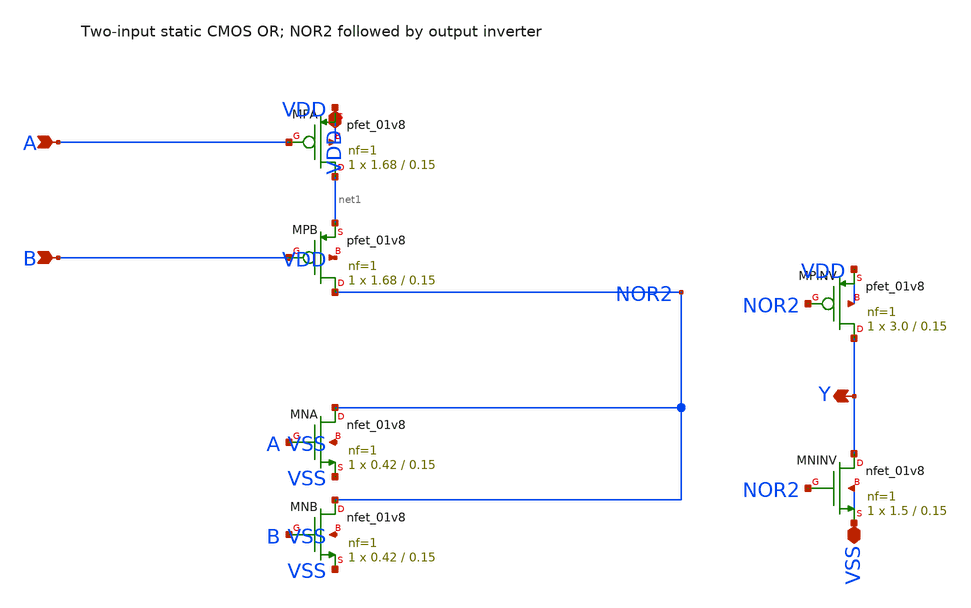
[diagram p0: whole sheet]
** sch_path: cells/control/phase_or2.sch
**.subckt phase_or2 VDD A B Y VSS
*.iopin VDD
*.ipin A
*.ipin B
*.opin Y
*.iopin VSS
XMPA net1 A VDD VDD sky130_fd_pr__pfet_01v8 L=0.15 W=1.68 nf=1 ad='int((nf+1)/2) * W/nf * 0.29' as='int((nf+2)/2) * W/nf * 0.29'
+ pd='2*int((nf+1)/2) * (W/nf + 0.29)' ps='2*int((nf+2)/2) * (W/nf + 0.29)' nrd='0.29 / W' nrs='0.29 / W'
+ sa=0 sb=0 sd=0 mult=1 m=1
XMPB NOR2 B net1 VDD sky130_fd_pr__pfet_01v8 L=0.15 W=1.68 nf=1 ad='int((nf+1)/2) * W/nf * 0.29' as='int((nf+2)/2) * W/nf * 0.29'
+ pd='2*int((nf+1)/2) * (W/nf + 0.29)' ps='2*int((nf+2)/2) * (W/nf + 0.29)' nrd='0.29 / W' nrs='0.29 / W'
+ sa=0 sb=0 sd=0 mult=1 m=1
XMNA NOR2 A VSS VSS sky130_fd_pr__nfet_01v8 L=0.15 W=0.42 nf=1 ad='int((1 + 1)/2) * 0.42 / 1 * 0.29'
+ as='int((1 + 2)/2) * 0.42 / 1 * 0.29' pd='2*int((1 + 1)/2) * (0.42 / 1 + 0.29)' ps='2*int((1 + 2)/2) * (0.42 / 1 + 0.29)'
+ nrd='0.29 / 0.42 ' nrs='0.29 / 0.42 ' sa=0 sb=0 sd=0 mult=1 m=1
XMNB NOR2 B VSS VSS sky130_fd_pr__nfet_01v8 L=0.15 W=0.42 nf=1 ad='int((1 + 1)/2) * 0.42 / 1 * 0.29'
+ as='int((1 + 2)/2) * 0.42 / 1 * 0.29' pd='2*int((1 + 1)/2) * (0.42 / 1 + 0.29)' ps='2*int((1 + 2)/2) * (0.42 / 1 + 0.29)'
+ nrd='0.29 / 0.42 ' nrs='0.29 / 0.42 ' sa=0 sb=0 sd=0 mult=1 m=1
XMPINV Y NOR2 VDD VDD sky130_fd_pr__pfet_01v8 L=0.15 W=3.0 nf=1 ad='int((nf+1)/2) * W/nf * 0.29' as='int((nf+2)/2) * W/nf * 0.29'
+ pd='2*int((nf+1)/2) * (W/nf + 0.29)' ps='2*int((nf+2)/2) * (W/nf + 0.29)' nrd='0.29 / W' nrs='0.29 / W'
+ sa=0 sb=0 sd=0 mult=1 m=1
XMNINV Y NOR2 VSS VSS sky130_fd_pr__nfet_01v8 L=0.15 W=1.5 nf=1 ad='int((1 + 1)/2) * 1.5 / 1 * 0.29'
+ as='int((1 + 2)/2) * 1.5 / 1 * 0.29' pd='2*int((1 + 1)/2) * (1.5 / 1 + 0.29)' ps='2*int((1 + 2)/2) * (1.5 / 1 + 0.29)'
+ nrd='0.29 / 1.5 ' nrs='0.29 / 1.5 ' sa=0 sb=0 sd=0 mult=1 m=1
**.ends
.end
